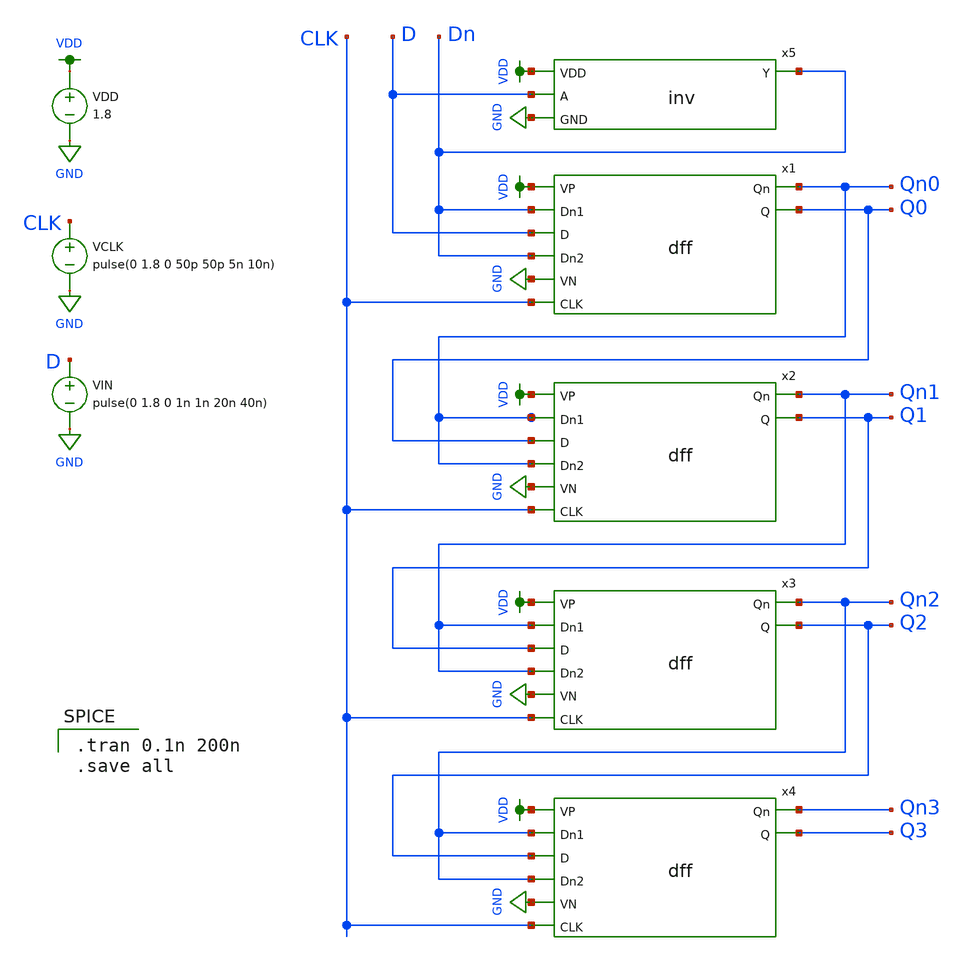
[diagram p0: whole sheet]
** sch_path: MP2/xschem/sreg_ff.sch
**.subckt sreg_ff
x1 VDD Dn Qn0 D Q0 Dn GND CLK dff
x2 VDD Qn0 Qn1 Q0 Q1 Qn0 GND CLK dff
x3 VDD Qn1 Qn2 Q1 Q2 Qn1 GND CLK dff
x4 VDD Qn2 Qn3 Q2 Q3 Qn2 GND CLK dff
x5 VDD D Dn GND inv
VDD VDD GND 1.8
VCLK CLK GND pulse(0 1.8 0 50p 50p 5n 10n)
VIN D GND pulse(0 1.8 0 1n 1n 20n 40n)
**** begin user architecture code

.tran 0.1n 200n
.save all


.lib $::SKYWATER_MODELS/sky130.lib.spice ff

**** end user architecture code
**.ends

* expanding   symbol:  /home/madvlsi/Desktop/MP2/xschem/dff.sym # of pins=8
** sym_path: MP2/xschem/dff.sym
** sch_path: MP2/xschem/dff.sch
.subckt dff VP Dn1 Qn D Q Dn2 VN CLK
*.opin Qn
*.opin Q
*.ipin Dn1
*.ipin D
*.ipin Dn2
*.ipin CLK
*.ipin VP
*.ipin VN
XM1 net1 Dn1 VP VDD sky130_fd_pr__pfet_01v8 L=0.15 W=1 nf=1 ad='int((nf+1)/2) * W/nf * 0.29' as='int((nf+2)/2) * W/nf * 0.29'
+ pd='2*int((nf+1)/2) * (W/nf + 0.29)' ps='2*int((nf+2)/2) * (W/nf + 0.29)' nrd='0.29 / W' nrs='0.29 / W'
+ sa=0 sb=0 sd=0 mult=1 m=1
XM2 net1 CLK VP VDD sky130_fd_pr__pfet_01v8 L=0.15 W=1 nf=1 ad='int((nf+1)/2) * W/nf * 0.29' as='int((nf+2)/2) * W/nf * 0.29'
+ pd='2*int((nf+1)/2) * (W/nf + 0.29)' ps='2*int((nf+2)/2) * (W/nf + 0.29)' nrd='0.29 / W' nrs='0.29 / W'
+ sa=0 sb=0 sd=0 mult=1 m=1
XM3 net7 net10 net1 VDD sky130_fd_pr__pfet_01v8 L=0.15 W=1 nf=1 ad='int((nf+1)/2) * W/nf * 0.29' as='int((nf+2)/2) * W/nf * 0.29'
+ pd='2*int((nf+1)/2) * (W/nf + 0.29)' ps='2*int((nf+2)/2) * (W/nf + 0.29)' nrd='0.29 / W' nrs='0.29 / W'
+ sa=0 sb=0 sd=0 mult=1 m=1
XM4 VP D net2 VDD sky130_fd_pr__pfet_01v8 L=0.15 W=1 nf=1 ad='int((nf+1)/2) * W/nf * 0.29' as='int((nf+2)/2) * W/nf * 0.29'
+ pd='2*int((nf+1)/2) * (W/nf + 0.29)' ps='2*int((nf+2)/2) * (W/nf + 0.29)' nrd='0.29 / W' nrs='0.29 / W'
+ sa=0 sb=0 sd=0 mult=1 m=1
XM5 net2 CLK VP VDD sky130_fd_pr__pfet_01v8 L=0.15 W=1 nf=1 ad='int((nf+1)/2) * W/nf * 0.29' as='int((nf+2)/2) * W/nf * 0.29'
+ pd='2*int((nf+1)/2) * (W/nf + 0.29)' ps='2*int((nf+2)/2) * (W/nf + 0.29)' nrd='0.29 / W' nrs='0.29 / W'
+ sa=0 sb=0 sd=0 mult=1 m=1
XM6 net10 net7 net2 VDD sky130_fd_pr__pfet_01v8 L=0.15 W=1 nf=1 ad='int((nf+1)/2) * W/nf * 0.29' as='int((nf+2)/2) * W/nf * 0.29'
+ pd='2*int((nf+1)/2) * (W/nf + 0.29)' ps='2*int((nf+2)/2) * (W/nf + 0.29)' nrd='0.29 / W' nrs='0.29 / W'
+ sa=0 sb=0 sd=0 mult=1 m=1
XM7 VP net7 net3 VDD sky130_fd_pr__pfet_01v8 L=0.15 W=1 nf=1 ad='int((nf+1)/2) * W/nf * 0.29' as='int((nf+2)/2) * W/nf * 0.29'
+ pd='2*int((nf+1)/2) * (W/nf + 0.29)' ps='2*int((nf+2)/2) * (W/nf + 0.29)' nrd='0.29 / W' nrs='0.29 / W'
+ sa=0 sb=0 sd=0 mult=1 m=1
XM8 Qn CLK net3 VDD sky130_fd_pr__pfet_01v8 L=0.15 W=1 nf=1 ad='int((nf+1)/2) * W/nf * 0.29' as='int((nf+2)/2) * W/nf * 0.29'
+ pd='2*int((nf+1)/2) * (W/nf + 0.29)' ps='2*int((nf+2)/2) * (W/nf + 0.29)' nrd='0.29 / W' nrs='0.29 / W'
+ sa=0 sb=0 sd=0 mult=1 m=1
XM9 VP Q Qn VDD sky130_fd_pr__pfet_01v8 L=0.15 W=1 nf=1 ad='int((nf+1)/2) * W/nf * 0.29' as='int((nf+2)/2) * W/nf * 0.29'
+ pd='2*int((nf+1)/2) * (W/nf + 0.29)' ps='2*int((nf+2)/2) * (W/nf + 0.29)' nrd='0.29 / W' nrs='0.29 / W'
+ sa=0 sb=0 sd=0 mult=1 m=1
XM10 net4 net10 VP VDD sky130_fd_pr__pfet_01v8 L=0.15 W=1 nf=1 ad='int((nf+1)/2) * W/nf * 0.29' as='int((nf+2)/2) * W/nf * 0.29'
+ pd='2*int((nf+1)/2) * (W/nf + 0.29)' ps='2*int((nf+2)/2) * (W/nf + 0.29)' nrd='0.29 / W' nrs='0.29 / W'
+ sa=0 sb=0 sd=0 mult=1 m=1
XM11 Q CLK net4 VDD sky130_fd_pr__pfet_01v8 L=0.15 W=1 nf=1 ad='int((nf+1)/2) * W/nf * 0.29' as='int((nf+2)/2) * W/nf * 0.29'
+ pd='2*int((nf+1)/2) * (W/nf + 0.29)' ps='2*int((nf+2)/2) * (W/nf + 0.29)' nrd='0.29 / W' nrs='0.29 / W'
+ sa=0 sb=0 sd=0 mult=1 m=1
XM12 VP Qn Q VDD sky130_fd_pr__pfet_01v8 L=0.15 W=1 nf=1 ad='int((nf+1)/2) * W/nf * 0.29' as='int((nf+2)/2) * W/nf * 0.29'
+ pd='2*int((nf+1)/2) * (W/nf + 0.29)' ps='2*int((nf+2)/2) * (W/nf + 0.29)' nrd='0.29 / W' nrs='0.29 / W'
+ sa=0 sb=0 sd=0 mult=1 m=1
XM13 net9 D VN GND sky130_fd_pr__nfet_01v8 L=0.15 W=1 nf=1 ad='int((nf+1)/2) * W/nf * 0.29' as='int((nf+2)/2) * W/nf * 0.29'
+ pd='2*int((nf+1)/2) * (W/nf + 0.29)' ps='2*int((nf+2)/2) * (W/nf + 0.29)' nrd='0.29 / W' nrs='0.29 / W'
+ sa=0 sb=0 sd=0 mult=1 m=1
XM14 net9 CLK net10 GND sky130_fd_pr__nfet_01v8 L=0.15 W=1 nf=1 ad='int((nf+1)/2) * W/nf * 0.29' as='int((nf+2)/2) * W/nf * 0.29'
+ pd='2*int((nf+1)/2) * (W/nf + 0.29)' ps='2*int((nf+2)/2) * (W/nf + 0.29)' nrd='0.29 / W' nrs='0.29 / W'
+ sa=0 sb=0 sd=0 mult=1 m=1
XM15 VN net7 net10 GND sky130_fd_pr__nfet_01v8 L=0.15 W=1 nf=1 ad='int((nf+1)/2) * W/nf * 0.29' as='int((nf+2)/2) * W/nf * 0.29'
+ pd='2*int((nf+1)/2) * (W/nf + 0.29)' ps='2*int((nf+2)/2) * (W/nf + 0.29)' nrd='0.29 / W' nrs='0.29 / W'
+ sa=0 sb=0 sd=0 mult=1 m=1
XM16 VN net10 net5 GND sky130_fd_pr__nfet_01v8 L=0.15 W=1 nf=1 ad='int((nf+1)/2) * W/nf * 0.29' as='int((nf+2)/2) * W/nf * 0.29'
+ pd='2*int((nf+1)/2) * (W/nf + 0.29)' ps='2*int((nf+2)/2) * (W/nf + 0.29)' nrd='0.29 / W' nrs='0.29 / W'
+ sa=0 sb=0 sd=0 mult=1 m=1
XM17 VN CLK net5 GND sky130_fd_pr__nfet_01v8 L=0.15 W=1 nf=1 ad='int((nf+1)/2) * W/nf * 0.29' as='int((nf+2)/2) * W/nf * 0.29'
+ pd='2*int((nf+1)/2) * (W/nf + 0.29)' ps='2*int((nf+2)/2) * (W/nf + 0.29)' nrd='0.29 / W' nrs='0.29 / W'
+ sa=0 sb=0 sd=0 mult=1 m=1
XM18 Q Qn net5 GND sky130_fd_pr__nfet_01v8 L=0.15 W=1 nf=1 ad='int((nf+1)/2) * W/nf * 0.29' as='int((nf+2)/2) * W/nf * 0.29'
+ pd='2*int((nf+1)/2) * (W/nf + 0.29)' ps='2*int((nf+2)/2) * (W/nf + 0.29)' nrd='0.29 / W' nrs='0.29 / W'
+ sa=0 sb=0 sd=0 mult=1 m=1
XM19 VN Dn2 net8 GND sky130_fd_pr__nfet_01v8 L=0.15 W=1 nf=1 ad='int((nf+1)/2) * W/nf * 0.29' as='int((nf+2)/2) * W/nf * 0.29'
+ pd='2*int((nf+1)/2) * (W/nf + 0.29)' ps='2*int((nf+2)/2) * (W/nf + 0.29)' nrd='0.29 / W' nrs='0.29 / W'
+ sa=0 sb=0 sd=0 mult=1 m=1
XM20 net8 CLK net7 GND sky130_fd_pr__nfet_01v8 L=0.15 W=1 nf=1 ad='int((nf+1)/2) * W/nf * 0.29' as='int((nf+2)/2) * W/nf * 0.29'
+ pd='2*int((nf+1)/2) * (W/nf + 0.29)' ps='2*int((nf+2)/2) * (W/nf + 0.29)' nrd='0.29 / W' nrs='0.29 / W'
+ sa=0 sb=0 sd=0 mult=1 m=1
XM21 VN net10 net7 GND sky130_fd_pr__nfet_01v8 L=0.15 W=1 nf=1 ad='int((nf+1)/2) * W/nf * 0.29' as='int((nf+2)/2) * W/nf * 0.29'
+ pd='2*int((nf+1)/2) * (W/nf + 0.29)' ps='2*int((nf+2)/2) * (W/nf + 0.29)' nrd='0.29 / W' nrs='0.29 / W'
+ sa=0 sb=0 sd=0 mult=1 m=1
XM22 net6 net7 VN GND sky130_fd_pr__nfet_01v8 L=0.15 W=1 nf=1 ad='int((nf+1)/2) * W/nf * 0.29' as='int((nf+2)/2) * W/nf * 0.29'
+ pd='2*int((nf+1)/2) * (W/nf + 0.29)' ps='2*int((nf+2)/2) * (W/nf + 0.29)' nrd='0.29 / W' nrs='0.29 / W'
+ sa=0 sb=0 sd=0 mult=1 m=1
XM23 VN CLK net6 GND sky130_fd_pr__nfet_01v8 L=0.15 W=1 nf=1 ad='int((nf+1)/2) * W/nf * 0.29' as='int((nf+2)/2) * W/nf * 0.29'
+ pd='2*int((nf+1)/2) * (W/nf + 0.29)' ps='2*int((nf+2)/2) * (W/nf + 0.29)' nrd='0.29 / W' nrs='0.29 / W'
+ sa=0 sb=0 sd=0 mult=1 m=1
XM24 Qn Q net6 GND sky130_fd_pr__nfet_01v8 L=0.15 W=1 nf=1 ad='int((nf+1)/2) * W/nf * 0.29' as='int((nf+2)/2) * W/nf * 0.29'
+ pd='2*int((nf+1)/2) * (W/nf + 0.29)' ps='2*int((nf+2)/2) * (W/nf + 0.29)' nrd='0.29 / W' nrs='0.29 / W'
+ sa=0 sb=0 sd=0 mult=1 m=1
.ends


* expanding   symbol:  /home/madvlsi/Desktop/MP2/xschem/inv.sym # of pins=4
** sym_path: MP2/xschem/inv.sym
** sch_path: MP2/xschem/inv.sch
.subckt inv VDD A Y GND
*.ipin A
*.opin Y
*.ipin VDD
*.ipin GND
XM1 Y A GND GND sky130_fd_pr__nfet_01v8 L=0.15 W=1 nf=1 ad='int((nf+1)/2) * W/nf * 0.29' as='int((nf+2)/2) * W/nf * 0.29'
+ pd='2*int((nf+1)/2) * (W/nf + 0.29)' ps='2*int((nf+2)/2) * (W/nf + 0.29)' nrd='0.29 / W' nrs='0.29 / W'
+ sa=0 sb=0 sd=0 mult=1 m=1
XM2 Y A VDD VDD sky130_fd_pr__pfet_01v8 L=0.15 W=1 nf=1 ad='int((nf+1)/2) * W/nf * 0.29' as='int((nf+2)/2) * W/nf * 0.29'
+ pd='2*int((nf+1)/2) * (W/nf + 0.29)' ps='2*int((nf+2)/2) * (W/nf + 0.29)' nrd='0.29 / W' nrs='0.29 / W'
+ sa=0 sb=0 sd=0 mult=1 m=1
.ends

.GLOBAL GND
.GLOBAL VDD
.end
